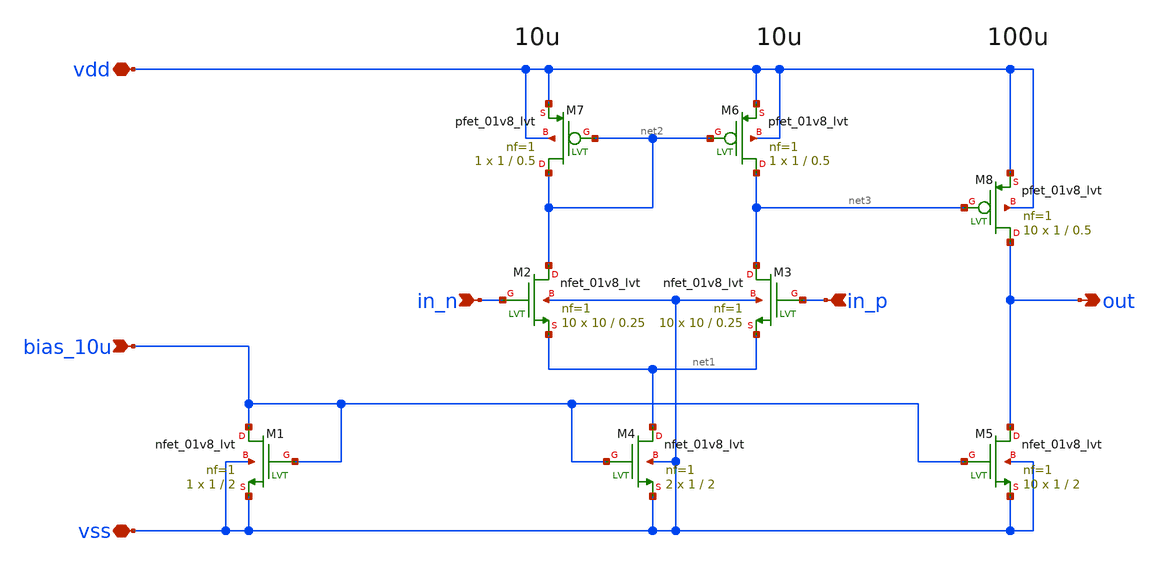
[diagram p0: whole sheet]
** sch_path: design/opamp/opamp.sch
**.subckt opamp vdd vss in_n in_p out bias_10u
*.iopin vdd
*.iopin vss
*.ipin in_n
*.ipin in_p
*.opin out
*.ipin bias_10u
XM1 bias_10u bias_10u vss vss sky130_fd_pr__nfet_01v8_lvt L=2 W=1 nf=1 ad='int((nf+1)/2) * W/nf * 0.29'
+ as='int((nf+2)/2) * W/nf * 0.29' pd='2*int((nf+1)/2) * (W/nf + 0.29)' ps='2*int((nf+2)/2) * (W/nf + 0.29)'
+ nrd='0.29 / W' nrs='0.29 / W' sa=0 sb=0 sd=0 mult=1 m=1
XM2 net2 in_n net1 vss sky130_fd_pr__nfet_01v8_lvt L=0.25 W=10 nf=1 ad='int((nf+1)/2) * W/nf * 0.29'
+ as='int((nf+2)/2) * W/nf * 0.29' pd='2*int((nf+1)/2) * (W/nf + 0.29)' ps='2*int((nf+2)/2) * (W/nf + 0.29)'
+ nrd='0.29 / W' nrs='0.29 / W' sa=0 sb=0 sd=0 mult=10 m=10
XM3 net3 in_p net1 vss sky130_fd_pr__nfet_01v8_lvt L=0.25 W=10 nf=1 ad='int((nf+1)/2) * W/nf * 0.29'
+ as='int((nf+2)/2) * W/nf * 0.29' pd='2*int((nf+1)/2) * (W/nf + 0.29)' ps='2*int((nf+2)/2) * (W/nf + 0.29)'
+ nrd='0.29 / W' nrs='0.29 / W' sa=0 sb=0 sd=0 mult=10 m=10
XM4 net1 bias_10u vss vss sky130_fd_pr__nfet_01v8_lvt L=2 W=1 nf=1 ad='int((nf+1)/2) * W/nf * 0.29' as='int((nf+2)/2) * W/nf * 0.29'
+ pd='2*int((nf+1)/2) * (W/nf + 0.29)' ps='2*int((nf+2)/2) * (W/nf + 0.29)' nrd='0.29 / W' nrs='0.29 / W'
+ sa=0 sb=0 sd=0 mult=2 m=2
XM5 out bias_10u vss vss sky130_fd_pr__nfet_01v8_lvt L=2 W=1 nf=1 ad='int((nf+1)/2) * W/nf * 0.29' as='int((nf+2)/2) * W/nf * 0.29'
+ pd='2*int((nf+1)/2) * (W/nf + 0.29)' ps='2*int((nf+2)/2) * (W/nf + 0.29)' nrd='0.29 / W' nrs='0.29 / W'
+ sa=0 sb=0 sd=0 mult=10 m=10
XM6 net3 net2 vdd vdd sky130_fd_pr__pfet_01v8_lvt L=0.5 W=1 nf=1 ad='int((nf+1)/2) * W/nf * 0.29' as='int((nf+2)/2) * W/nf * 0.29'
+ pd='2*int((nf+1)/2) * (W/nf + 0.29)' ps='2*int((nf+2)/2) * (W/nf + 0.29)' nrd='0.29 / W' nrs='0.29 / W'
+ sa=0 sb=0 sd=0 mult=1 m=1
XM7 net2 net2 vdd vdd sky130_fd_pr__pfet_01v8_lvt L=0.5 W=1 nf=1 ad='int((nf+1)/2) * W/nf * 0.29' as='int((nf+2)/2) * W/nf * 0.29'
+ pd='2*int((nf+1)/2) * (W/nf + 0.29)' ps='2*int((nf+2)/2) * (W/nf + 0.29)' nrd='0.29 / W' nrs='0.29 / W'
+ sa=0 sb=0 sd=0 mult=1 m=1
XM8 out net3 vdd vdd sky130_fd_pr__pfet_01v8_lvt L=0.5 W=1 nf=1 ad='int((nf+1)/2) * W/nf * 0.29' as='int((nf+2)/2) * W/nf * 0.29'
+ pd='2*int((nf+1)/2) * (W/nf + 0.29)' ps='2*int((nf+2)/2) * (W/nf + 0.29)' nrd='0.29 / W' nrs='0.29 / W'
+ sa=0 sb=0 sd=0 mult=10 m=10
**.ends
.end
